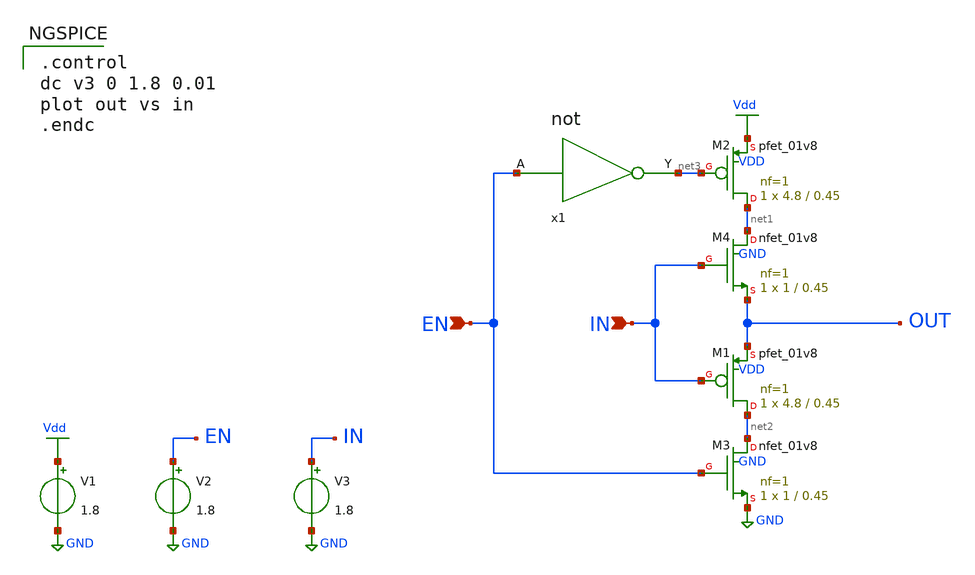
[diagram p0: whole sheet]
** sch_path: Circuiti/memories/tests.sch
**.subckt tests IN EN
*.ipin IN
*.ipin EN
V1 Vdd GND 1.8
XM2 net1 net3 Vdd VDD sky130_fd_pr__pfet_01v8 L=0.45 W=4.8 nf=1 ad='int((nf+1)/2) * W/nf * 0.29' as='int((nf+2)/2) * W/nf * 0.29'
+ pd='2*int((nf+1)/2) * (W/nf + 0.29)' ps='2*int((nf+2)/2) * (W/nf + 0.29)' nrd='0.29 / W' nrs='0.29 / W'
+ sa=0 sb=0 sd=0 mult=1 m=1
XM3 net2 EN GND GND sky130_fd_pr__nfet_01v8 L=0.45 W=1 nf=1 ad='int((nf+1)/2) * W/nf * 0.29' as='int((nf+2)/2) * W/nf * 0.29'
+ pd='2*int((nf+1)/2) * (W/nf + 0.29)' ps='2*int((nf+2)/2) * (W/nf + 0.29)' nrd='0.29 / W' nrs='0.29 / W'
+ sa=0 sb=0 sd=0 mult=1 m=1
x1 EN net3 not
V2 EN GND 1.8
V3 IN GND 1.8
XM1 net2 IN OUT VDD sky130_fd_pr__pfet_01v8 L=0.45 W=4.8 nf=1 ad='int((nf+1)/2) * W/nf * 0.29' as='int((nf+2)/2) * W/nf * 0.29'
+ pd='2*int((nf+1)/2) * (W/nf + 0.29)' ps='2*int((nf+2)/2) * (W/nf + 0.29)' nrd='0.29 / W' nrs='0.29 / W'
+ sa=0 sb=0 sd=0 mult=1 m=1
XM4 net1 IN OUT GND sky130_fd_pr__nfet_01v8 L=0.45 W=1 nf=1 ad='int((nf+1)/2) * W/nf * 0.29' as='int((nf+2)/2) * W/nf * 0.29'
+ pd='2*int((nf+1)/2) * (W/nf + 0.29)' ps='2*int((nf+2)/2) * (W/nf + 0.29)' nrd='0.29 / W' nrs='0.29 / W'
+ sa=0 sb=0 sd=0 mult=1 m=1
**** begin user architecture code


.lib /home/matteo/xschem_downloads/skywater-pdk/libraries/sky130_fd_pr_ngspice/latest/models/sky130.lib.spice tt

*.include /home/matteo/xschem_downloads/skywater-pdk/libraries/sky130_fd_pr_ngspice/latest/cells/nfet_01v8/sky130_fd_pr__nfet_01v8__tt.corner.spice

.param mc_mm_switch=0
.param mc_pr_switch=1



.control
dc v3 0 1.8 0.01
plot out vs in
.endc



.ic v(r1)=0
.ic v(r2)=0
.ic v(r3)=0
.ic v(r4)=0

**** end user architecture code
**.ends

* expanding   symbol:  /home/matteo/Documenti/tesi/Circuiti/logic_gates_sch_sym/not.sym # of pins=2
** sym_path: Circuiti/logic_gates_sch_sym/not.sym
** sch_path: Circuiti/logic_gates_sch_sym/not.sch
.subckt not A Y
*.ipin A
*.opin Y
XM1 Y A GND GND sky130_fd_pr__nfet_01v8 L=0.45 W=1 nf=1 ad='int((nf+1)/2) * W/nf * 0.29' as='int((nf+2)/2) * W/nf * 0.29'
+ pd='2*int((nf+1)/2) * (W/nf + 0.29)' ps='2*int((nf+2)/2) * (W/nf + 0.29)' nrd='0.29 / W' nrs='0.29 / W'
+ sa=0 sb=0 sd=0 mult=1 m=1
XM2 Y A Vdd VDD sky130_fd_pr__pfet_01v8 L=0.45 W=4.8 nf=1 ad='int((nf+1)/2) * W/nf * 0.29' as='int((nf+2)/2) * W/nf * 0.29'
+ pd='2*int((nf+1)/2) * (W/nf + 0.29)' ps='2*int((nf+2)/2) * (W/nf + 0.29)' nrd='0.29 / W' nrs='0.29 / W'
+ sa=0 sb=0 sd=0 mult=1 m=1
.ends

.GLOBAL GND
.GLOBAL Vdd
.end
